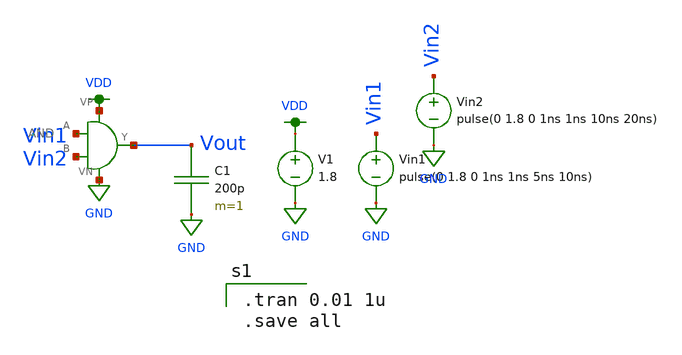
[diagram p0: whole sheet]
** sch_path: Homework1/AND_tran.sch
**.subckt AND_tran
V1 VDD GND 1.8
Vin1 Vin1 GND pulse(0 1.8 0 1ns 1ns 5ns 10ns)
Vin2 Vin2 GND pulse(0 1.8 0 1ns 1ns 10ns 20ns)
C1 Vout GND 200p m=1
X1 Vin1 Vin2 VDD GND Vout AND
**** begin user architecture code

.option wnflag=1
.lib ~/skywater/skywater-pdk/libraries/sky130_fd_pr_ngspice/latest/models/sky130.lib.spice tt


.tran 0.01 1u
.save all

**** end user architecture code
**.ends

* expanding   symbol:  /home/madvlsi/Documents/MADVLSI/Homework1/AND.sym # of pins=5
** sym_path: Homework1/AND.sym
** sch_path: Homework1/AND.sch
.subckt AND A B VP VN Y
*.iopin VP
*.iopin VN
*.ipin A
*.ipin B
*.opin Y
X1 A VP VN net1 B NAND
X2 net1 VP VN Y inverter
.ends


* expanding   symbol:  /home/madvlsi/Documents/MADVLSI/Homework1/NAND.sym # of pins=5
** sym_path: Homework1/NAND.sym
** sch_path: Homework1/NAND.sch
.subckt NAND A VP VN Y B
*.ipin A
*.iopin VP
*.ipin B
*.iopin VN
*.opin Y
XM1 Y A net1 VN sky130_fd_pr__nfet_01v8 L=0.15 W=1 nf=1 ad='int((nf+1)/2) * W/nf * 0.29' as='int((nf+2)/2) * W/nf * 0.29'
+ pd='2*int((nf+1)/2) * (W/nf + 0.29)' ps='2*int((nf+2)/2) * (W/nf + 0.29)' nrd='0.29 / W' nrs='0.29 / W'
+ sa=0 sb=0 sd=0 mult=1 m=1
XM2 Y A VP VP sky130_fd_pr__pfet_01v8 L=0.15 W=1 nf=1 ad='int((nf+1)/2) * W/nf * 0.29' as='int((nf+2)/2) * W/nf * 0.29'
+ pd='2*int((nf+1)/2) * (W/nf + 0.29)' ps='2*int((nf+2)/2) * (W/nf + 0.29)' nrd='0.29 / W' nrs='0.29 / W'
+ sa=0 sb=0 sd=0 mult=1 m=1
XM6 Y B VP VP sky130_fd_pr__pfet_01v8 L=0.15 W=1 nf=1 ad='int((nf+1)/2) * W/nf * 0.29' as='int((nf+2)/2) * W/nf * 0.29'
+ pd='2*int((nf+1)/2) * (W/nf + 0.29)' ps='2*int((nf+2)/2) * (W/nf + 0.29)' nrd='0.29 / W' nrs='0.29 / W'
+ sa=0 sb=0 sd=0 mult=1 m=1
XM3 net1 B VN VN sky130_fd_pr__nfet_01v8 L=0.15 W=1 nf=1 ad='int((nf+1)/2) * W/nf * 0.29' as='int((nf+2)/2) * W/nf * 0.29'
+ pd='2*int((nf+1)/2) * (W/nf + 0.29)' ps='2*int((nf+2)/2) * (W/nf + 0.29)' nrd='0.29 / W' nrs='0.29 / W'
+ sa=0 sb=0 sd=0 mult=1 m=1
.ends


* expanding   symbol:  /home/madvlsi/Documents/MADVLSI/Homework1/inverter.sym # of pins=4
** sym_path: Homework1/inverter.sym
** sch_path: Homework1/inverter.sch
.subckt inverter A VP VN Y
*.ipin A
*.iopin VP
*.iopin VN
*.opin Y
XM1 Y A VN VN sky130_fd_pr__nfet_01v8 L=0.15 W=1 nf=1 ad='int((nf+1)/2) * W/nf * 0.29' as='int((nf+2)/2) * W/nf * 0.29'
+ pd='2*int((nf+1)/2) * (W/nf + 0.29)' ps='2*int((nf+2)/2) * (W/nf + 0.29)' nrd='0.29 / W' nrs='0.29 / W'
+ sa=0 sb=0 sd=0 mult=1 m=1
XM2 Y A VP VP sky130_fd_pr__pfet_01v8 L=0.15 W=1 nf=1 ad='int((nf+1)/2) * W/nf * 0.29' as='int((nf+2)/2) * W/nf * 0.29'
+ pd='2*int((nf+1)/2) * (W/nf + 0.29)' ps='2*int((nf+2)/2) * (W/nf + 0.29)' nrd='0.29 / W' nrs='0.29 / W'
+ sa=0 sb=0 sd=0 mult=1 m=1
.ends

.GLOBAL VDD
.GLOBAL GND
.end
